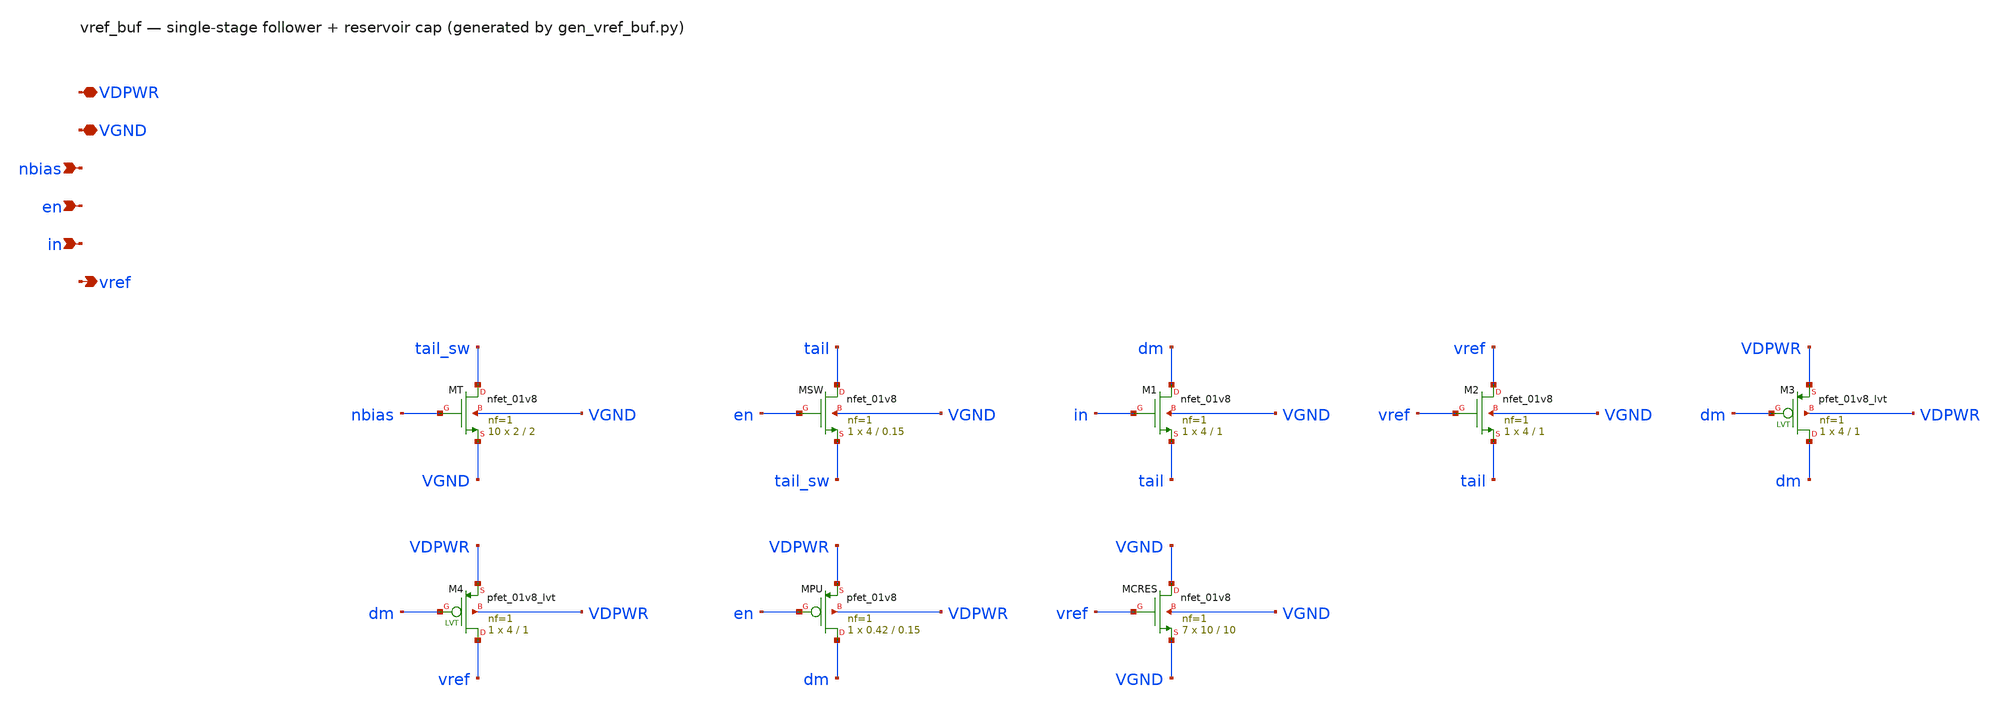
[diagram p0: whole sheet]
** sch_path: xschem/vref_buf.sch
**.subckt vref_buf VDPWR VGND nbias en in vref
*.iopin VDPWR
*.iopin VGND
*.ipin nbias
*.ipin en
*.ipin in
*.opin vref
XMT tail_sw nbias VGND VGND sky130_fd_pr__nfet_01v8 L=2 W=2 nf=1 ad='int((1 + 1)/2) * 2 / 1 * 0.29' as='int((1 + 2)/2) * 2 / 1 * 0.29'
+ pd='2*int((1 + 1)/2) * (2 / 1 + 0.29)' ps='2*int((1 + 2)/2) * (2 / 1 + 0.29)' nrd='0.29 / 2 ' nrs='0.29 / 2 '
+ sa=0 sb=0 sd=0 mult=10 m=10
XMSW tail en tail_sw VGND sky130_fd_pr__nfet_01v8 L=0.15 W=4 nf=1 ad='int((1 + 1)/2) * 4 / 1 * 0.29'
+ as='int((1 + 2)/2) * 4 / 1 * 0.29' pd='2*int((1 + 1)/2) * (4 / 1 + 0.29)' ps='2*int((1 + 2)/2) * (4 / 1 + 0.29)'
+ nrd='0.29 / 4 ' nrs='0.29 / 4 ' sa=0 sb=0 sd=0 mult=1 m=1
XM1 dm in tail VGND sky130_fd_pr__nfet_01v8 L=1 W=4 nf=1 ad='int((1 + 1)/2) * 4 / 1 * 0.29' as='int((1 + 2)/2) * 4 / 1 * 0.29'
+ pd='2*int((1 + 1)/2) * (4 / 1 + 0.29)' ps='2*int((1 + 2)/2) * (4 / 1 + 0.29)' nrd='0.29 / 4 ' nrs='0.29 / 4 '
+ sa=0 sb=0 sd=0 mult=1 m=1
XM2 vref vref tail VGND sky130_fd_pr__nfet_01v8 L=1 W=4 nf=1 ad='int((1 + 1)/2) * 4 / 1 * 0.29' as='int((1 + 2)/2) * 4 / 1 * 0.29'
+ pd='2*int((1 + 1)/2) * (4 / 1 + 0.29)' ps='2*int((1 + 2)/2) * (4 / 1 + 0.29)' nrd='0.29 / 4 ' nrs='0.29 / 4 '
+ sa=0 sb=0 sd=0 mult=1 m=1
XM3 dm dm VDPWR VDPWR sky130_fd_pr__pfet_01v8_lvt L=1 W=4 nf=1 ad='int((1 + 1)/2) * 4 / 1 * 0.29' as='int((1 + 2)/2) * 4 / 1 * 0.29'
+ pd='2*int((1 + 1)/2) * (4 / 1 + 0.29)' ps='2*int((1 + 2)/2) * (4 / 1 + 0.29)' nrd='0.29 / 4 ' nrs='0.29 / 4 '
+ sa=0 sb=0 sd=0 mult=1 m=1
XM4 vref dm VDPWR VDPWR sky130_fd_pr__pfet_01v8_lvt L=1 W=4 nf=1 ad='int((1 + 1)/2) * 4 / 1 * 0.29' as='int((1 + 2)/2) * 4 / 1 * 0.29'
+ pd='2*int((1 + 1)/2) * (4 / 1 + 0.29)' ps='2*int((1 + 2)/2) * (4 / 1 + 0.29)' nrd='0.29 / 4 ' nrs='0.29 / 4 '
+ sa=0 sb=0 sd=0 mult=1 m=1
XMPU dm en VDPWR VDPWR sky130_fd_pr__pfet_01v8 L=0.15 W=0.42 nf=1 ad='int((nf+1)/2) * W/nf * 0.29' as='int((nf+2)/2) * W/nf * 0.29'
+ pd='2*int((nf+1)/2) * (W/nf + 0.29)' ps='2*int((nf+2)/2) * (W/nf + 0.29)' nrd='0.29 / W' nrs='0.29 / W'
+ sa=0 sb=0 sd=0 mult=1 m=1
XMCRES VGND vref VGND VGND sky130_fd_pr__nfet_01v8 L=10 W=10 nf=1 ad='int((1 + 1)/2) * 10 / 1 * 0.29'
+ as='int((1 + 2)/2) * 10 / 1 * 0.29' pd='2*int((1 + 1)/2) * (10 / 1 + 0.29)' ps='2*int((1 + 2)/2) * (10 / 1 + 0.29)'
+ nrd='0.29 / 10 ' nrs='0.29 / 10 ' sa=0 sb=0 sd=0 mult=7 m=7
**.ends
.end
